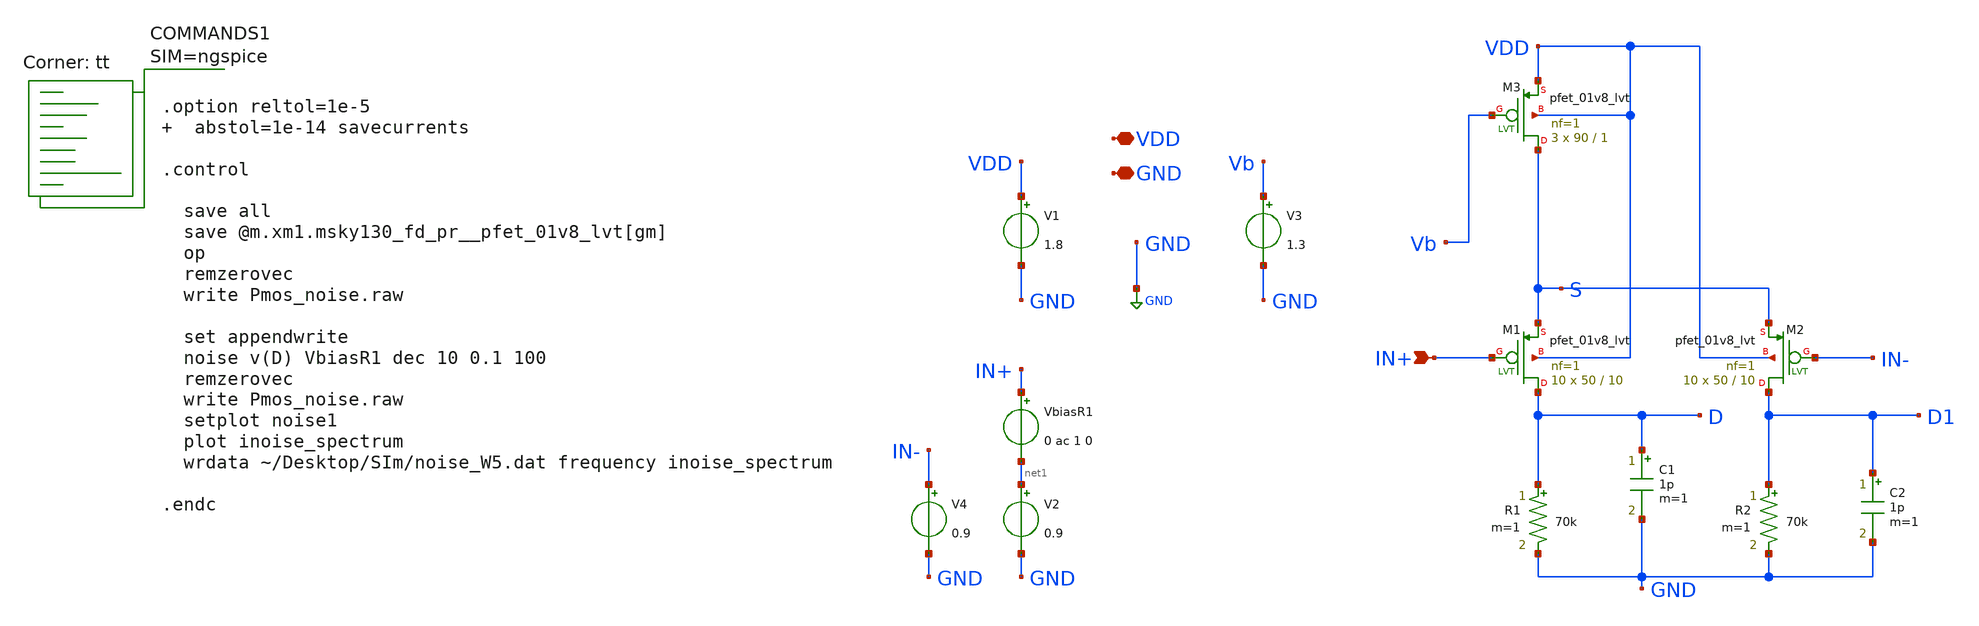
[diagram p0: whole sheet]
** sch_path: xschem/Pmos_noise.sch
**.subckt Pmos_noise VDD GND IN+
*.iopin VDD
*.iopin GND
*.ipin IN+
VbiasR1 IN+ net1 0 ac 1 0
V2 net1 GND 0.9
V1 VDD GND 1.8
C1 D GND 1p m=1
XM1 D IN+ S VDD sky130_fd_pr__pfet_01v8_lvt L=10 W=50 nf=1 ad='int((nf+1)/2) * W/nf * 0.29' as='int((nf+2)/2) * W/nf * 0.29'
+ pd='2*int((nf+1)/2) * (W/nf + 0.29)' ps='2*int((nf+2)/2) * (W/nf + 0.29)' nrd='0.29 / W' nrs='0.29 / W'
+ sa=0 sb=0 sd=0 mult=10 m=10
V3 Vb GND 1.3
R1 D GND 70k m=1
XM3 S Vb VDD VDD sky130_fd_pr__pfet_01v8_lvt L=1 W=90 nf=1 ad='int((nf+1)/2) * W/nf * 0.29' as='int((nf+2)/2) * W/nf * 0.29'
+ pd='2*int((nf+1)/2) * (W/nf + 0.29)' ps='2*int((nf+2)/2) * (W/nf + 0.29)' nrd='0.29 / W' nrs='0.29 / W'
+ sa=0 sb=0 sd=0 mult=3 m=3
XM2 D1 IN- S VDD sky130_fd_pr__pfet_01v8_lvt L=10 W=50 nf=1 ad='int((nf+1)/2) * W/nf * 0.29' as='int((nf+2)/2) * W/nf * 0.29'
+ pd='2*int((nf+1)/2) * (W/nf + 0.29)' ps='2*int((nf+2)/2) * (W/nf + 0.29)' nrd='0.29 / W' nrs='0.29 / W'
+ sa=0 sb=0 sd=0 mult=10 m=10
V4 IN- GND 0.9
R2 D1 GND 70k m=1
C2 D1 GND 1p m=1
**** begin user architecture code



.option reltol=1e-5   abstol=1e-14 savecurrents

.control

  save all
  save @m.xm1.msky130_fd_pr__pfet_01v8_lvt[gm]
  op
  remzerovec
  write Pmos_noise.raw

  set appendwrite
  noise v(D) VbiasR1 dec 10 0.1 100
  remzerovec
  write Pmos_noise.raw
  setplot noise1
  plot inoise_spectrum
  wrdata ~/Desktop/SIm/noise_W5.dat frequency inoise_spectrum

.endc



.lib $::SKYWATER_MODELS/sky130.lib.spice tt
**** end user architecture code
**.ends
.GLOBAL GND
.end
